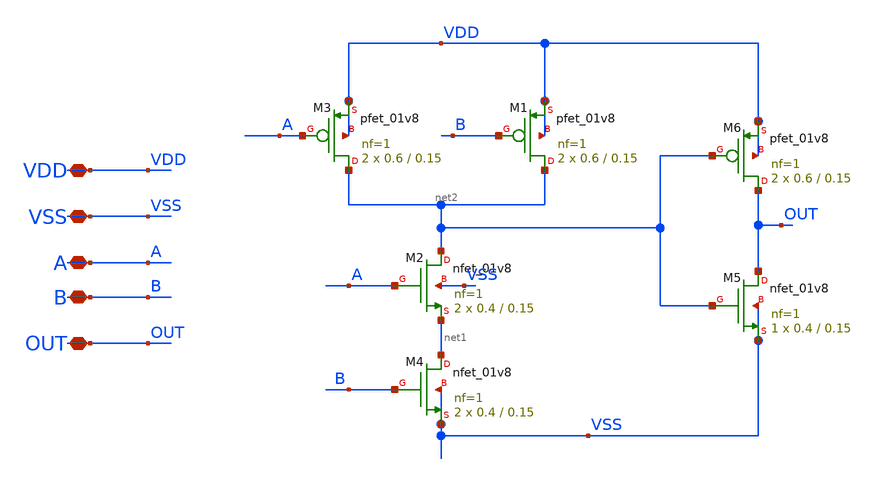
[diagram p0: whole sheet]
** sch_path: xschem/DC_DC_Converter_xschem/DC_DC_Converter/Delay_block_revised/AND_GATE/AND.sch
**.subckt AND VDD VSS A B OUT
*.iopin VDD
*.iopin VSS
*.iopin A
*.iopin B
*.iopin OUT
XM2 net2 A net1 VSS sky130_fd_pr__nfet_01v8 L=0.15 W=0.4 nf=1 ad='int((nf+1)/2) * W/nf * 0.29' as='int((nf+2)/2) * W/nf * 0.29'
+ pd='2*int((nf+1)/2) * (W/nf + 0.29)' ps='2*int((nf+2)/2) * (W/nf + 0.29)' nrd='0.29 / W' nrs='0.29 / W'
+ sa=0 sb=0 sd=0 mult=2 m=2
XM3 net2 A VDD VDD sky130_fd_pr__pfet_01v8 L=0.15 W=0.6 nf=1 ad='int((nf+1)/2) * W/nf * 0.29' as='int((nf+2)/2) * W/nf * 0.29'
+ pd='2*int((nf+1)/2) * (W/nf + 0.29)' ps='2*int((nf+2)/2) * (W/nf + 0.29)' nrd='0.29 / W' nrs='0.29 / W'
+ sa=0 sb=0 sd=0 mult=2 m=2
XM4 net1 B VSS VSS sky130_fd_pr__nfet_01v8 L=0.15 W=0.4 nf=1 ad='int((nf+1)/2) * W/nf * 0.29' as='int((nf+2)/2) * W/nf * 0.29'
+ pd='2*int((nf+1)/2) * (W/nf + 0.29)' ps='2*int((nf+2)/2) * (W/nf + 0.29)' nrd='0.29 / W' nrs='0.29 / W'
+ sa=0 sb=0 sd=0 mult=2 m=2
XM5 OUT net2 VSS VSS sky130_fd_pr__nfet_01v8 L=0.15 W=0.4 nf=1 ad='int((nf+1)/2) * W/nf * 0.29' as='int((nf+2)/2) * W/nf * 0.29'
+ pd='2*int((nf+1)/2) * (W/nf + 0.29)' ps='2*int((nf+2)/2) * (W/nf + 0.29)' nrd='0.29 / W' nrs='0.29 / W'
+ sa=0 sb=0 sd=0 mult=1 m=1
XM1 net2 B VDD VDD sky130_fd_pr__pfet_01v8 L=0.15 W=0.6 nf=1 ad='int((nf+1)/2) * W/nf * 0.29' as='int((nf+2)/2) * W/nf * 0.29'
+ pd='2*int((nf+1)/2) * (W/nf + 0.29)' ps='2*int((nf+2)/2) * (W/nf + 0.29)' nrd='0.29 / W' nrs='0.29 / W'
+ sa=0 sb=0 sd=0 mult=2 m=2
XM6 OUT net2 VDD VDD sky130_fd_pr__pfet_01v8 L=0.15 W=0.6 nf=1 ad='int((nf+1)/2) * W/nf * 0.29' as='int((nf+2)/2) * W/nf * 0.29'
+ pd='2*int((nf+1)/2) * (W/nf + 0.29)' ps='2*int((nf+2)/2) * (W/nf + 0.29)' nrd='0.29 / W' nrs='0.29 / W'
+ sa=0 sb=0 sd=0 mult=2 m=2
**.ends
.end
